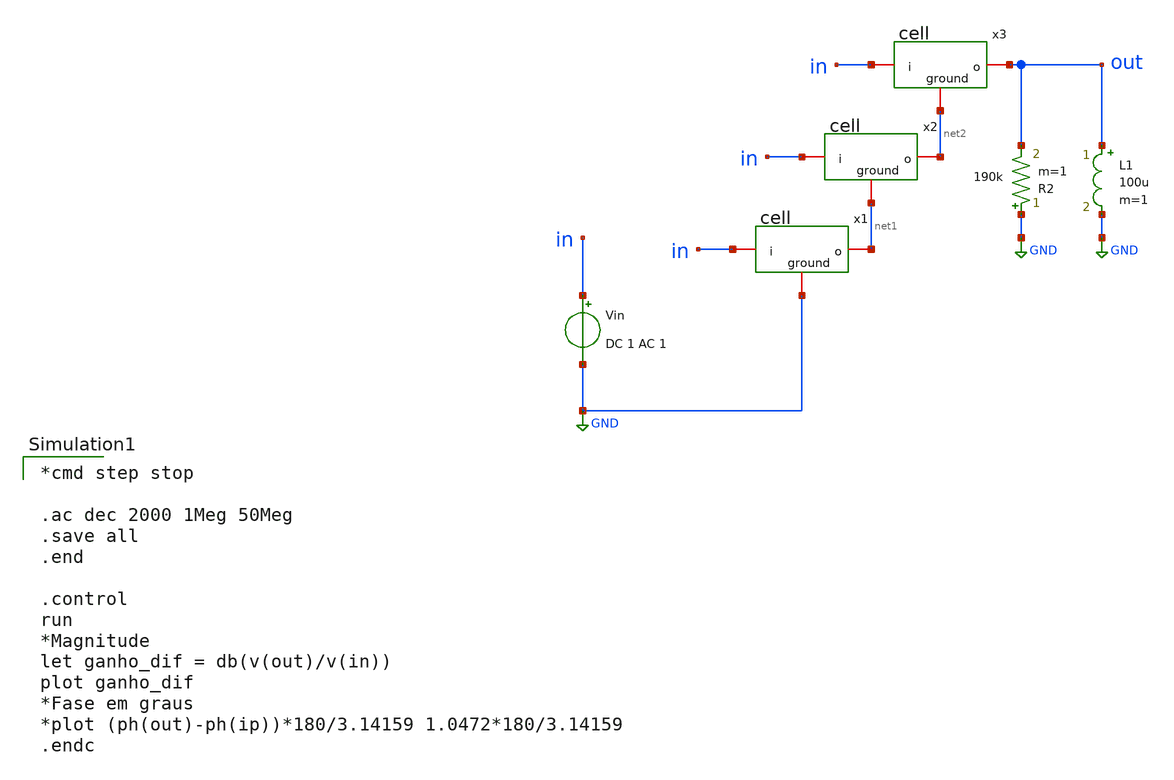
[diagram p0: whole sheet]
** sch_path: xschem/matching/multiplier-full-3-cap.sch
**.subckt multiplier-full-3-cap
x1 net1 in GND cell
x2 net2 in net1 cell
R2 GND out 190k m=1
x3 out in net2 cell
Vin in GND DC 1 AC 1
L1 out GND 100u m=1
**** begin user architecture code

** opencircuitdesign pdks install
.lib $::SKYWATER_MODELS/sky130.lib.spice tt



*cmd step stop

.ac dec 2000 1Meg 50Meg
.save all
.end

.control
run
*Magnitude
let ganho_dif = db(v(out)/v(in))
plot ganho_dif
*Fase em graus
*plot (ph(out)-ph(ip))*180/3.14159 1.0472*180/3.14159
.endc

**** end user architecture code
**.ends

* expanding   symbol:  cell.sym # of pins=3
** sym_path: xschem/cell.sym
** sch_path: xschem/cell.sch
.subckt cell o i ground
*.iopin ground
*.iopin o
*.iopin i
XM10 net1 net1 ground net1 sky130_fd_pr__pfet_01v8_lvt L=0.35 W=40 nf=5 ad='int((5 + 1)/2) * 40 / 5 * 0.29'
+ as='int((5 + 2)/2) * 40 / 5 * 0.29' pd='2*int((5 + 1)/2) * (40 / 5 + 0.29)' ps='2*int((5 + 2)/2) * (40 / 5 + 0.29)'
+ nrd='0.29 / 40 ' nrs='0.29 / 40 ' sa=0 sb=0 sd=0 mult=1 m=1
XM1 o o net1 o sky130_fd_pr__pfet_01v8_lvt L=0.35 W=40 nf=5 ad='int((5 + 1)/2) * 40 / 5 * 0.29' as='int((5 + 2)/2) * 40 / 5 * 0.29'
+ pd='2*int((5 + 1)/2) * (40 / 5 + 0.29)' ps='2*int((5 + 2)/2) * (40 / 5 + 0.29)' nrd='0.29 / 40 ' nrs='0.29 / 40 '
+ sa=0 sb=0 sd=0 mult=1 m=1
XC3 o ground sky130_fd_pr__cap_mim_m3_1 W=30 L=30 MF=3 m=3
XC2 net1 i sky130_fd_pr__cap_mim_m3_1 W=30 L=30 MF=1 m=1
.ends

.GLOBAL GND
.end
